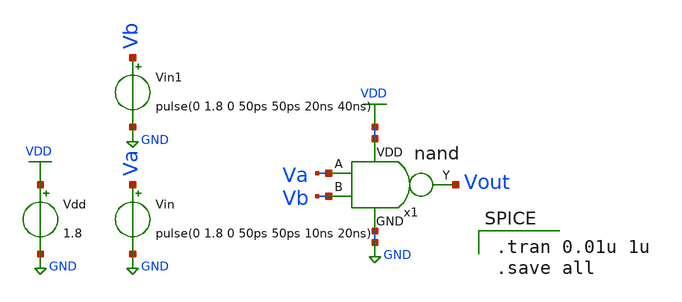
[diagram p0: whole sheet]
** sch_path: designs/or/xschem/or_tb.sch
**.subckt or_tb
Vdd VDD GND 1.8
Vin Va GND pulse(0 1.8 0 50ps 50ps 10ns 20ns)
x1 VDD Va Vb Vout GND nand
Vin1 Vb GND pulse(0 1.8 0 50ps 50ps 20ns 40ns)
**** begin user architecture code

** opencircuidesign pdks install
.lib /home/ubvm/Desktop/chip_design/open_pdks/sky130/sky130A/libs.tech/ngspice/sky130.lib.spice tt_mm




.tran 0.01u 1u
.save all

**** end user architecture code
**.ends

* expanding   symbol:  /home/ubvm/unic-cass/nand/nand.sym # of pins=5
** sym_path: designs/nand/xschem/nand.sym
** sch_path: designs/nand/xschem/nand.sch
.subckt nand VDD A B Y GND
input p1
input p2
output p3
inout p4
inout p5
XM1 net2 net5 net4 net4 sky130_fd_pr__nfet_01v8 L=0.15 W=1 nf=1 ad='int((1 + 1)/2) * 1 / 1 * 0.29' as='int((1 + 2)/2) * 1 / 1 * 0.29'
+ pd='2*int((1 + 1)/2) * (1 / 1 + 0.29)' ps='2*int((1 + 2)/2) * (1 / 1 + 0.29)' nrd='0.29 / 1 ' nrs='0.29 / 1 '
+ sa=0 sb=0 sd=0 mult=1 m=1
XM2 net2 net6 net1 net1 sky130_fd_pr__pfet_01v8 L=0.15 W=1 nf=1 ad='int((1 + 1)/2) * 1 / 1 * 0.29' as='int((1 + 2)/2) * 1 / 1 * 0.29'
+ pd='2*int((1 + 1)/2) * (1 / 1 + 0.29)' ps='2*int((1 + 2)/2) * (1 / 1 + 0.29)' nrd='0.29 / 1 ' nrs='0.29 / 1 '
+ sa=0 sb=0 sd=0 mult=1 m=1
XM3 net1 net5 net3 net3 sky130_fd_pr__pfet_01v8 L=0.15 W=1 nf=1 ad='int((1 + 1)/2) * 1 / 1 * 0.29' as='int((1 + 2)/2) * 1 / 1 * 0.29'
+ pd='2*int((1 + 1)/2) * (1 / 1 + 0.29)' ps='2*int((1 + 2)/2) * (1 / 1 + 0.29)' nrd='0.29 / 1 ' nrs='0.29 / 1 '
+ sa=0 sb=0 sd=0 mult=1 m=1
XM4 net2 net6 net4 net4 sky130_fd_pr__nfet_01v8 L=0.15 W=1 nf=1 ad='int((1 + 1)/2) * 1 / 1 * 0.29' as='int((1 + 2)/2) * 1 / 1 * 0.29'
+ pd='2*int((1 + 1)/2) * (1 / 1 + 0.29)' ps='2*int((1 + 2)/2) * (1 / 1 + 0.29)' nrd='0.29 / 1 ' nrs='0.29 / 1 '
+ sa=0 sb=0 sd=0 mult=1 m=1
.ends

.GLOBAL VDD
.GLOBAL GND
.end
